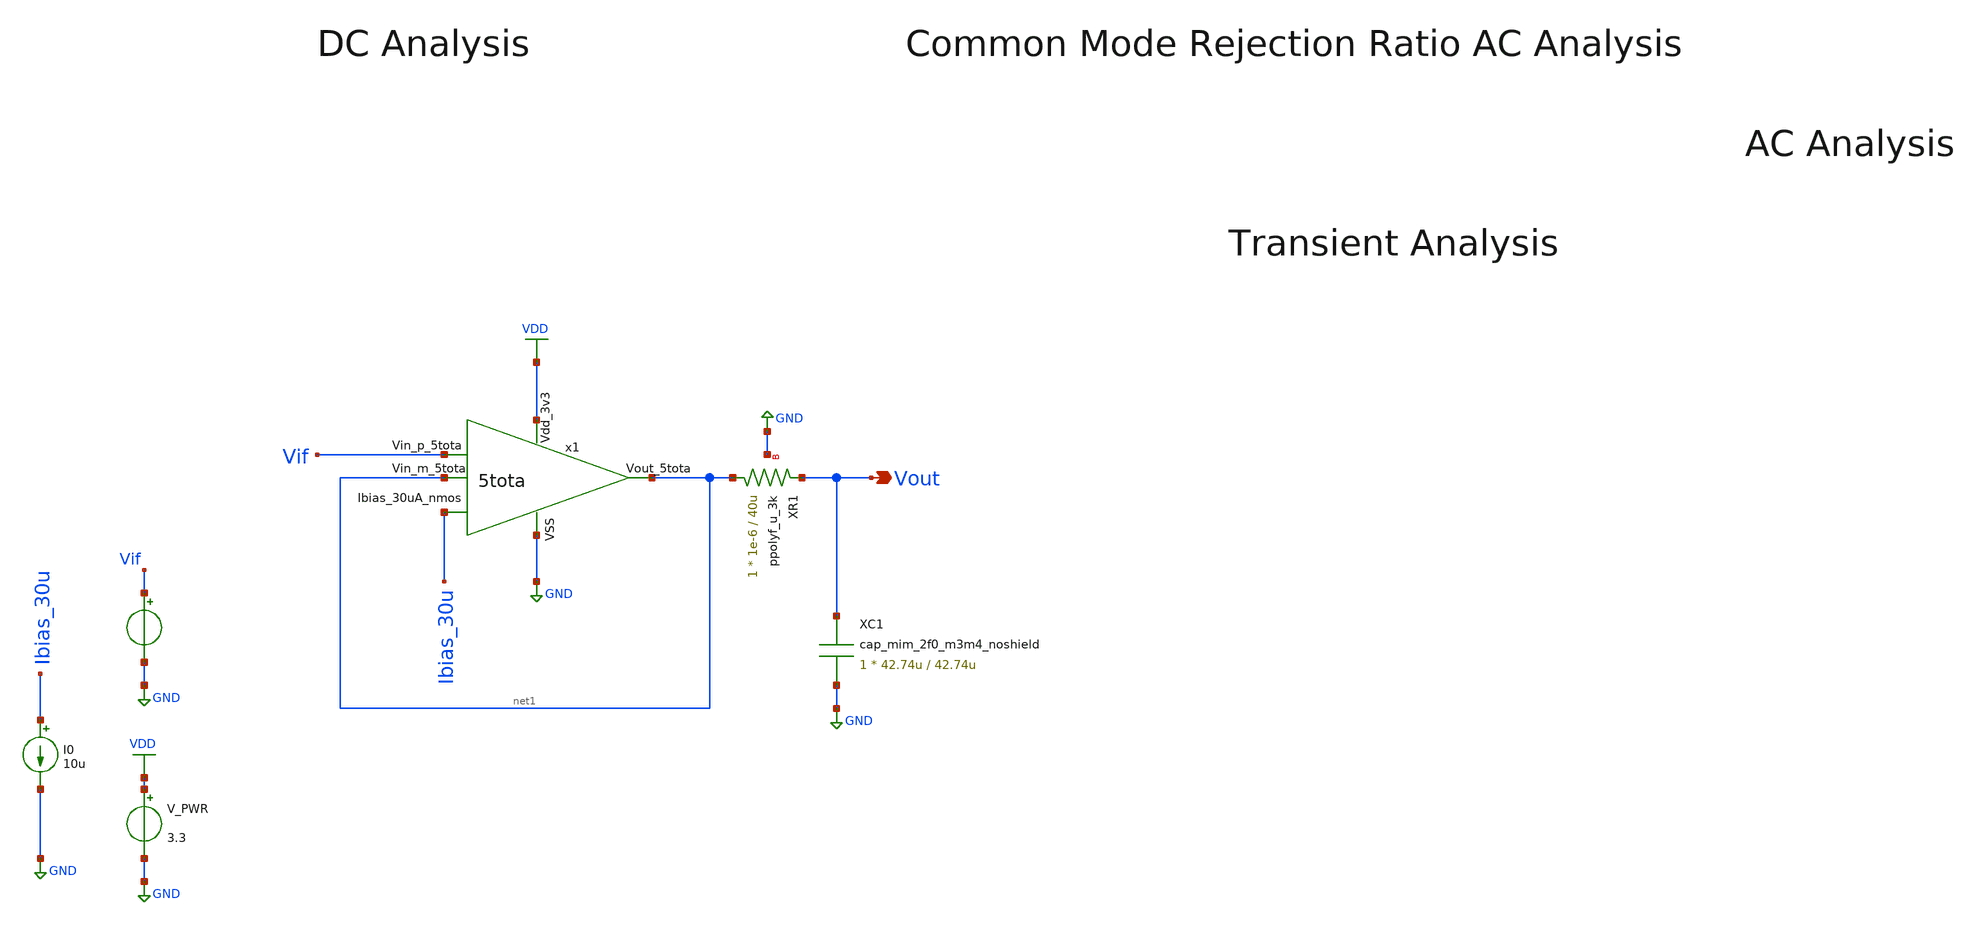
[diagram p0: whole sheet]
** sch_path: Analog/schematics/2_mixer/low_pass_filter_tb.sch
**.subckt low_pass_filter_tb Vout
*.opin Vout
V_PWR VDD GND 3.3
.save i(v_pwr)
V_IF Vif GND sin( 1 1 1 0 )
.save i(v_if)
I0 Ibias_30u GND 10u
x1 VDD net1 Vif net1 GND Ibias_30u 5tota
XC1 Vout GND cap_mim_2f0_m3m4_noshield c_width=42.74u c_length=42.74u m=1
XR1 net1 Vout GND ppolyf_u_3k r_width=1e-6 r_length=40u m=1
**** begin user architecture code

.include $::180MCU_MODELS/design.ngspice
.lib $::180MCU_MODELS/sm141064.ngspice typical
.lib $::180MCU_MODELS/sm141064.ngspice mimcap_typical
.lib $::180MCU_MODELS/sm141064.ngspice cap_mim
.lib $::180MCU_MODELS/sm141064.ngspice res_typical




* Complete 5T OTA + RC Low-Pass Filter Verification Testbench

.control
    * ==========================================
    * SETUP CONFIGURATIONS & GLOBAL VARIABLES
    * ==========================================
    set freq_if = 312k
    set cm_if   = 2.0
    set amp_if  = 0.1

    * Pre-allocate vector space for clean file writing
    save all

    * ==========================================
    * TEST 1: DC OPERATING POINT (Closed-Loop)
    * ==========================================
    * Configure input as a DC source for common-mode tracking sweep
    alter @V_IF[sin]   = [ 2.0 0 0 0 ]

    * Sweep the common mode from 0V to VDD (3.3V supply)
    dc V_IF 0 3.3 0.05

    * Scripted calculation to check where closed-loop gain tracks close to 1.0 (Unity)
    setplot dc1
    let ota_dc_gain = deriv(v(Vout))
    *** plot ota_dc_gain xlimit 1.0 3.0 title 'Filter DC Closed-Loop Gain vs Input Common Mode'

    set appendwrite = 0
    write /workspace/Analog/schematics/2_mixer/simulation_files/5tota_lpf_tb_dc.raw

    * Show operating parameters of the OTA transistors at the nominal 2.0V common-mode
    show all

    * ==========================================
    * TEST 2: AC ANALYSIS (FILTER CHARACTERISTIC)
    * ==========================================
    * Reset DC level to nominal 2.0V, apply single-ended AC magnitude of 1.0
    alter @V_IF[dc]    = $cm_if
    alter @V_IF[acmag]  = 1.0

    * Run AC analysis across a wide frequency grid
    ac dec 10 1 10G

    setplot ac1
    let mag_db = db(v(Vout))
    let phase_deg = ph(v(Vout)) * 180 / pi

    *** plot mag_db title 'Closed-Loop Filter AC Magnitude Response'
    *** plot phase_deg title 'Closed-Loop Filter AC Phase Response'

    set appendwrite = 0
    write /workspace/Analog/schematics/2_mixer/simulation_files/5tota_lpf_tb_ac.raw

    * ==========================================
    * TEST 3: TRANSIENT ANALYSIS
    * ==========================================
    * Reconfigure single-ended voltage source to deliver the baseband frequency
    alter @V_IF[sin]   = [ $cm_if $amp_if $freq_if 0 ]

    * Run transient simulation (300u duration covers ~93 full cycles of 312kHz)
    tran 3n 300u

    setplot tran1
    *** plot v(Vif) v(Vout_5tota) v(Vout) title 'Transient Filter Waveforms'

    set appendwrite = 0
    write /workspace/Analog/schematics/2_mixer/simulation_files/5tota_lpf_tb_tran.raw

    * ==========================================
    * TEST 4: CLOSED-LOOP AC RESPONSE (Populates CMRR Box)
    * ==========================================
    * To prevent an empty grid, we populate this file with a fine-grained sweep
    * of the filter's output magnitude response.
    alter @V_IF[dc]    = $cm_if
    alter @V_IF[acmag]  = 1.0

    ac dec 10 1 100meg

    setplot ac2
    let cmrr_db = ac1.mag_db
    *** plot cmrr_db title 'Filter Closed-Loop AC Response'

    set appendwrite = 0
    write /workspace/Analog/schematics/2_mixer/simulation_files/5tota_lpf_tb_cmrr.raw

    * ==========================================
    * TEST 5: NOISE ANALYSIS (Filter Output Noise Window)
    * ==========================================
    * Calculate input-referred and output noise across the filter bandwidth window
    *noise v(Vout) V_IF dec 10 10 10meg

    *setplot noise1
    *plot db(onoise_spectrum) db(inoise_spectrum) title 'Filter Output and Input-Referred Noise (V^2/Hz)'

    * ==========================================
    * DATA EXPORT
    * ==========================================
    *echo '=== Exporting all filter simulation plots to separate raw files complete ==='

.endc


**** end user architecture code
**.ends

* expanding   symbol:  Analog/schematics/2_mixer/5tota.sym # of pins=6
** sym_path: Analog/schematics/2_mixer/5tota.sym
** sch_path: Analog/schematics/2_mixer/5tota.sch
.subckt 5tota Vdd_3v3 Vout_5tota Vin_p_5tota Vin_m_5tota VSS Ibias_30uA_nmos
*.ipin Vdd_3v3
*.ipin Vin_p_5tota
*.ipin Vin_m_5tota
*.opin Vout_5tota
*.iopin Ibias_30uA_nmos
*.ipin VSS
XMnmos_amp_p net1 Vin_p_5tota Ibias_30uA_nmos VSS nfet_03v3 L=0.28u W=6u nf=1 ad='int((nf+1)/2) * W/nf
+ * 0.18u' as='int((nf+2)/2) * W/nf * 0.18u' pd='2*int((nf+1)/2) * (W/nf + 0.18u)' ps='2*int((nf+2)/2)
+ * (W/nf + 0.18u)' nrd='0.18u / W' nrs='0.18u / W' sa=0 sb=0 sd=0 m=1
XMnmos_amp_n Vout_5tota Vin_m_5tota Ibias_30uA_nmos VSS nfet_03v3 L=0.28u W=6u nf=1 ad='int((nf+1)/2)
+ * W/nf * 0.18u' as='int((nf+2)/2) * W/nf * 0.18u' pd='2*int((nf+1)/2) * (W/nf + 0.18u)' ps='2*int((nf+2)/2)
+ * (W/nf + 0.18u)' nrd='0.18u / W' nrs='0.18u / W' sa=0 sb=0 sd=0 m=1
XMpmos_cs_p net1 net1 Vdd_3v3 VDD pfet_03v3 L=0.28u W=10u nf=1 ad='int((nf+1)/2) * W/nf * 0.18u' as='int((nf+2)/2)
+ * W/nf * 0.18u' pd='2*int((nf+1)/2) * (W/nf + 0.18u)' ps='2*int((nf+2)/2) * (W/nf + 0.18u)' nrd='0.18u
+ / W' nrs='0.18u / W' sa=0 sb=0 sd=0 m=1
XMpmos_cs_n Vout_5tota net1 Vdd_3v3 VDD pfet_03v3 L=0.28u W=10u nf=1 ad='int((nf+1)/2) * W/nf * 0.18u' as='int((nf+2)/2)
+ * W/nf * 0.18u' pd='2*int((nf+1)/2) * (W/nf + 0.18u)' ps='2*int((nf+2)/2) * (W/nf + 0.18u)' nrd='0.18u
+ / W' nrs='0.18u / W' sa=0 sb=0 sd=0 m=1
.ends

.GLOBAL VDD
.GLOBAL GND
.end
